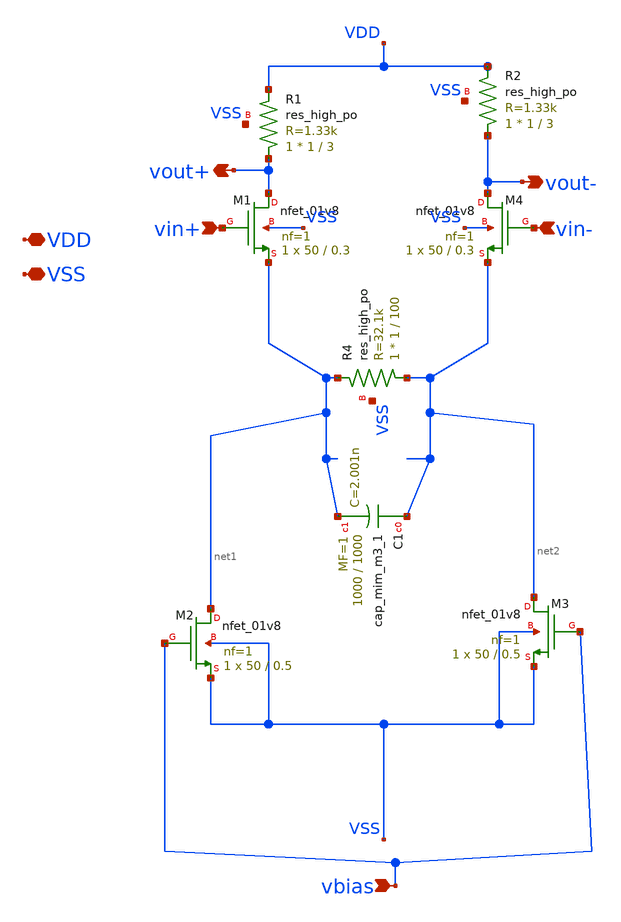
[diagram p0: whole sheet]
** sch_path: xschem/CTLE.sch
**.subckt CTLE VDD VSS vin+ vin- vout- vout+ vbias
*.iopin VDD
*.iopin VSS
*.ipin vin+
*.ipin vin-
*.opin vout-
*.opin vout+
*.ipin vbias
XM1 vout+ vin+ net1 VSS sky130_fd_pr__nfet_01v8 L=0.3 W=50 nf=1 ad='int((nf+1)/2) * W/nf * 0.29' as='int((nf+2)/2) * W/nf * 0.29'
+ pd='2*int((nf+1)/2) * (W/nf + 0.29)' ps='2*int((nf+2)/2) * (W/nf + 0.29)' nrd='0.29 / W' nrs='0.29 / W'
+ sa=0 sb=0 sd=0 mult=1 m=1
XM2 net1 vbias VSS VSS sky130_fd_pr__nfet_01v8 L=0.5 W=50 nf=1 ad='int((nf+1)/2) * W/nf * 0.29' as='int((nf+2)/2) * W/nf * 0.29'
+ pd='2*int((nf+1)/2) * (W/nf + 0.29)' ps='2*int((nf+2)/2) * (W/nf + 0.29)' nrd='0.29 / W' nrs='0.29 / W'
+ sa=0 sb=0 sd=0 mult=1 m=1
XM4 vout- vin- net2 VSS sky130_fd_pr__nfet_01v8 L=0.3 W=50 nf=1 ad='int((nf+1)/2) * W/nf * 0.29' as='int((nf+2)/2) * W/nf * 0.29'
+ pd='2*int((nf+1)/2) * (W/nf + 0.29)' ps='2*int((nf+2)/2) * (W/nf + 0.29)' nrd='0.29 / W' nrs='0.29 / W'
+ sa=0 sb=0 sd=0 mult=1 m=1
XR1 vout+ VDD VSS sky130_fd_pr__res_high_po W=1 L=3 mult=1 m=1
XR2 vout- VDD VSS sky130_fd_pr__res_high_po W=1 L=3 mult=1 m=1
XR4 net2 net1 VSS sky130_fd_pr__res_high_po W=1 L=100 mult=1 m=1
XC1 net2 net1 sky130_fd_pr__cap_mim_m3_1 W=1000 L=1000 MF=1 m=1
XM3 net2 vbias VSS VSS sky130_fd_pr__nfet_01v8 L=0.5 W=50 nf=1 ad='int((nf+1)/2) * W/nf * 0.29' as='int((nf+2)/2) * W/nf * 0.29'
+ pd='2*int((nf+1)/2) * (W/nf + 0.29)' ps='2*int((nf+2)/2) * (W/nf + 0.29)' nrd='0.29 / W' nrs='0.29 / W'
+ sa=0 sb=0 sd=0 mult=1 m=1
**.ends
.end
